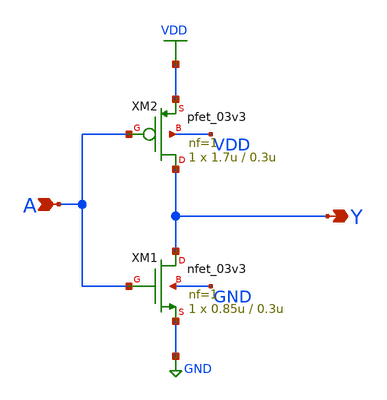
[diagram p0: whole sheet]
** sch_path: designs/globalfoundries-pdk-libs-gf180mcu_osu_sc/gf180mcu_osu_sc_gp9t3v3/cells/inv/gf180mcu_osu_sc_gp9t3v3__inv_1.sch
**.subckt gf180mcu_osu_sc_gp9t3v3__inv_1 A Y
*.ipin A
*.opin Y
XM1 Y A GND GND nfet_03v3 L=0.3u W=0.85u nf=1 ad='int((nf+1)/2) * W/nf * 0.18u' as='int((nf+2)/2) * W/nf * 0.18u'
+ pd='2*int((nf+1)/2) * (W/nf + 0.18u)' ps='2*int((nf+2)/2) * (W/nf + 0.18u)' nrd='0.18u / W' nrs='0.18u / W'
+ sa=0 sb=0 sd=0 m=1
XM2 Y A VDD VDD pfet_03v3 L=0.3u W=1.7u nf=1 ad='int((nf+1)/2) * W/nf * 0.18u' as='int((nf+2)/2) * W/nf * 0.18u'
+ pd='2*int((nf+1)/2) * (W/nf + 0.18u)' ps='2*int((nf+2)/2) * (W/nf + 0.18u)' nrd='0.18u / W' nrs='0.18u / W'
+ sa=0 sb=0 sd=0 m=1
**.ends
.GLOBAL VDD
.GLOBAL GND
.end
